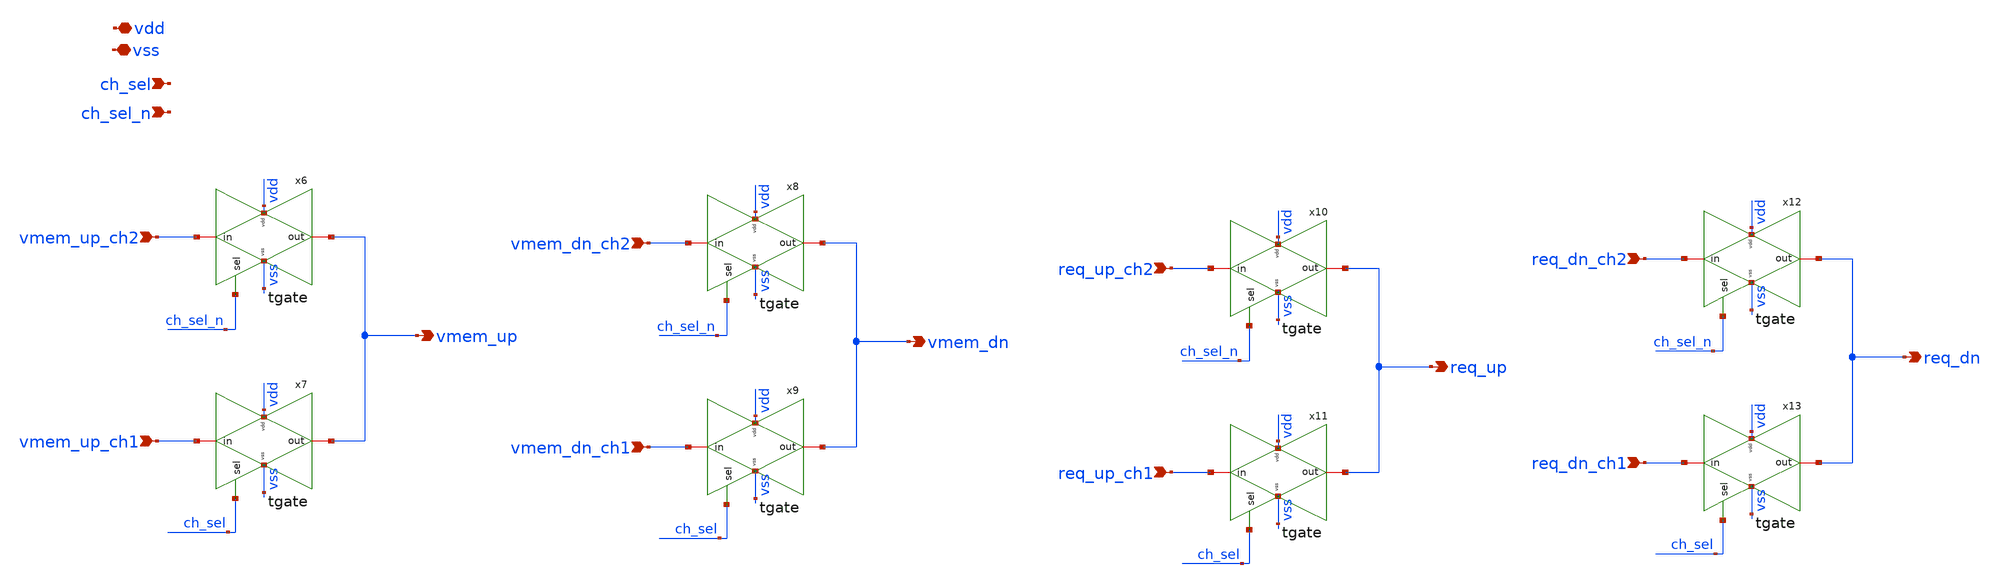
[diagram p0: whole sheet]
** sch_path: v2_feature_extr/output_sel_R.sch
**.subckt output_sel_R ch_sel vdd vss vmem_up vmem_up_ch2 vmem_up_ch1 vmem_dn vmem_dn_ch2
*+ vmem_dn_ch1 req_up req_up_ch2 req_up_ch1 req_dn req_dn_ch2 req_dn_ch1 ch_sel_n
*.ipin ch_sel
*.iopin vdd
*.iopin vss
*.opin vmem_up
*.ipin vmem_up_ch2
*.ipin vmem_up_ch1
*.opin vmem_dn
*.ipin vmem_dn_ch2
*.ipin vmem_dn_ch1
*.opin req_up
*.ipin req_up_ch2
*.ipin req_up_ch1
*.opin req_dn
*.ipin req_dn_ch2
*.ipin req_dn_ch1
*.ipin ch_sel_n
x6 vss vdd vmem_up_ch2 vmem_up ch_sel_n tgate
x7 vss vdd vmem_up_ch1 vmem_up ch_sel tgate
x8 vss vdd vmem_dn_ch2 vmem_dn ch_sel_n tgate
x9 vss vdd vmem_dn_ch1 vmem_dn ch_sel tgate
x10 vss vdd req_up_ch2 req_up ch_sel_n tgate
x11 vss vdd req_up_ch1 req_up ch_sel tgate
x12 vss vdd req_dn_ch2 req_dn ch_sel_n tgate
x13 vss vdd req_dn_ch1 req_dn ch_sel tgate
**.ends
.end
